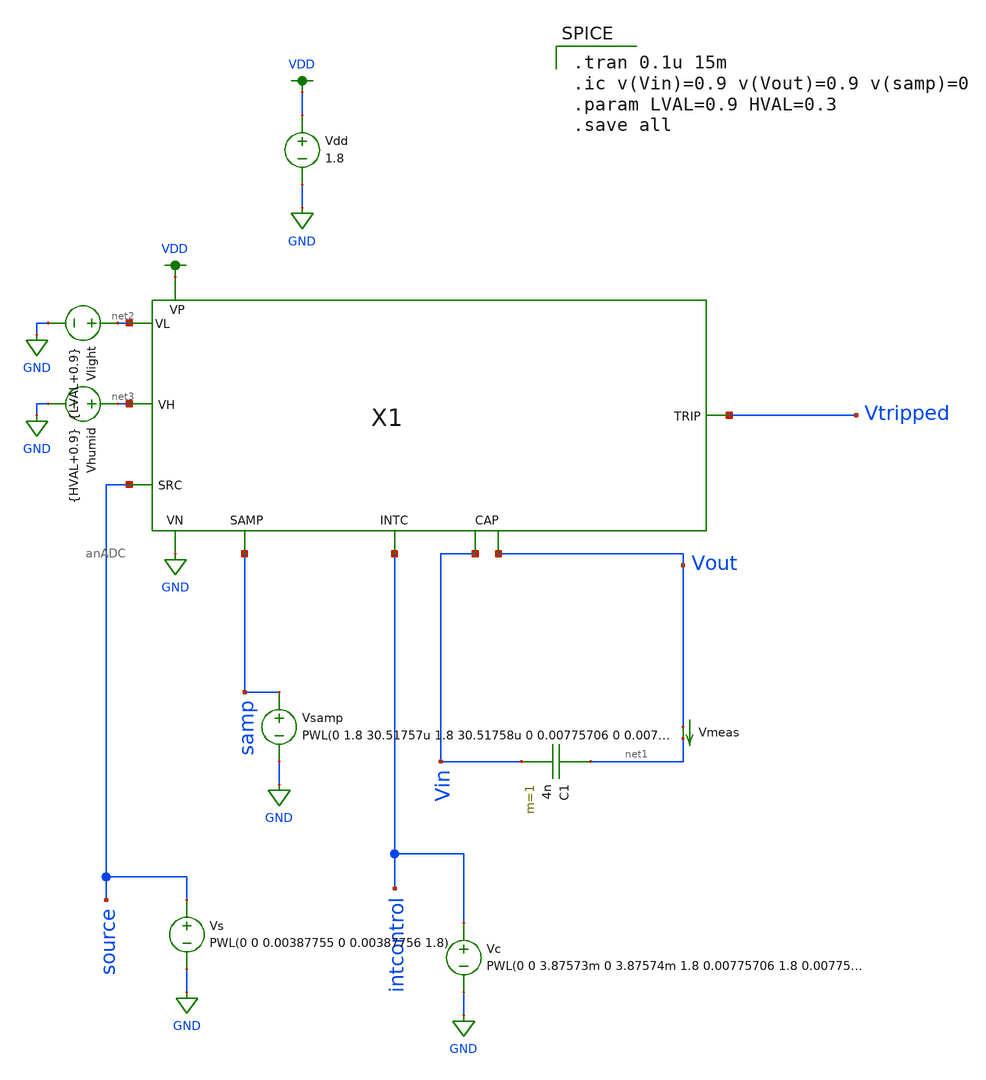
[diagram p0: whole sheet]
** sch_path: analog/anADC_test.sch
**.subckt anADC_test
Vdd VDD GND 1.8
C1 net1 Vin 4n m=1
Vlight net2 GND {LVAL+0.9}
Vmeas Vout net1 0
.save i(vmeas)
Vhumid net3 GND {HVAL+0.9}
Vs source GND PWL(0 0 0.00387755 0 0.00387756 1.8)
Vc intcontrol GND PWL(0 0 3.87573m 0 3.87574m 1.8 0.00775706 1.8 0.007757061 0 0.01163461 0
+ 0.01163462 1.8)
Vsamp samp GND PWL(0 1.8 30.51757u 1.8 30.51758u 0 0.00775706 0 0.007757061 1.8 0.00778757 1.8
+ 0.00778758 0)
X1 Vtripped Vout Vin intcontrol samp source net3 net2 anADC
**** begin user architecture code

.option wnflag=1
.param MC_SWITCH=0.0
.lib ~/skywater/skywater-pdk/libraries/sky130_fd_pr_ngspice/latest/models/sky130.lib.spice tt


.tran 0.1u 15m
.ic v(Vin)=0.9 v(Vout)=0.9 v(samp)=0
.param LVAL=0.9 HVAL=0.3
.save all

**** end user architecture code
**.ends

* expanding   symbol:  /home/jonah/VLSI/final/anADC.sym # of pins=8
** sym_path: analog/anADC.sym
** sch_path: analog/anADC.sch
.subckt anADC Vtrip OCC2 OCC1 intc Samp Source VH VL
*.iopin OCC1
*.iopin OCC2
*.iopin VL
*.iopin VH
*.ipin Samp
*.ipin Source
*.ipin intc
*.opin Vtrip
X4 net1 OCC2 net10 net3 GND VDD sbc2
X7 net1 OCC1 net2 OCC2 GND VDD sbc2
XM5 VDD net3 Vtrip VDD sky130_fd_pr__pfet_01v8 L=0.15 W=3 nf=1 ad='int((nf+1)/2) * W/nf * 0.29' as='int((nf+2)/2) * W/nf * 0.29'
+ pd='2*int((nf+1)/2) * (W/nf + 0.29)' ps='2*int((nf+2)/2) * (W/nf + 0.29)' nrd='0.29 / W' nrs='0.29 / W'
+ sa=0 sb=0 sd=0 mult=1 m=1
XM6 Vtrip net3 GND GND sky130_fd_pr__nfet_01v8 L=0.15 W=3 nf=1 ad='int((nf+1)/2) * W/nf * 0.29' as='int((nf+2)/2) * W/nf * 0.29'
+ pd='2*int((nf+1)/2) * (W/nf + 0.29)' ps='2*int((nf+2)/2) * (W/nf + 0.29)' nrd='0.29 / W' nrs='0.29 / W'
+ sa=0 sb=0 sd=0 mult=1 m=1
X8 net5 GND net4 VDD GND intc amux
X9 net8 net5 net6 net5 GND VDD sbc2
XR1 OCC1 net4 GND sky130_fd_pr__res_xhigh_po W=0.35 L=175.2 mult=1 m=1
XR2 net1 VDD GND sky130_fd_pr__res_xhigh_po W=0.35 L=194 mult=1 m=1
XR3 GND net1 GND sky130_fd_pr__res_xhigh_po W=0.35 L=194 mult=1 m=1
XM3 net7 Samp net8 GND sky130_fd_pr__nfet_01v8 L=0.15 W=5 nf=1 ad='int((nf+1)/2) * W/nf * 0.29' as='int((nf+2)/2) * W/nf * 0.29'
+ pd='2*int((nf+1)/2) * (W/nf + 0.29)' ps='2*int((nf+2)/2) * (W/nf + 0.29)' nrd='0.29 / W' nrs='0.29 / W'
+ sa=0 sb=0 sd=0 mult=1 m=1
X6 VL VH net7 VDD GND Source amux
XM4 net7 net9 net8 VDD sky130_fd_pr__pfet_01v8 L=0.15 W=5 nf=1 ad='int((nf+1)/2) * W/nf * 0.29' as='int((nf+2)/2) * W/nf * 0.29'
+ pd='2*int((nf+1)/2) * (W/nf + 0.29)' ps='2*int((nf+2)/2) * (W/nf + 0.29)' nrd='0.29 / W' nrs='0.29 / W'
+ sa=0 sb=0 sd=0 mult=1 m=1
XM1 GND Samp net9 GND sky130_fd_pr__nfet_01v8 L=0.15 W=1 nf=1 ad='int((nf+1)/2) * W/nf * 0.29' as='int((nf+2)/2) * W/nf * 0.29'
+ pd='2*int((nf+1)/2) * (W/nf + 0.29)' ps='2*int((nf+2)/2) * (W/nf + 0.29)' nrd='0.29 / W' nrs='0.29 / W'
+ sa=0 sb=0 sd=0 mult=1 m=1
XM2 VDD Samp net9 VDD sky130_fd_pr__pfet_01v8 L=0.15 W=1 nf=1 ad='int((nf+1)/2) * W/nf * 0.29' as='int((nf+2)/2) * W/nf * 0.29'
+ pd='2*int((nf+1)/2) * (W/nf + 0.29)' ps='2*int((nf+2)/2) * (W/nf + 0.29)' nrd='0.29 / W' nrs='0.29 / W'
+ sa=0 sb=0 sd=0 mult=1 m=1
XC2 net2 OCC2 sky130_fd_pr__cap_mim_m3_1 W=25 L=10 MF=1 m=1
XC1 net5 net6 sky130_fd_pr__cap_mim_m3_1 W=25 L=10 MF=1 m=1
XC3 net8 GND sky130_fd_pr__cap_mim_m3_1 W=25 L=20 MF=1 m=1
.ends


* expanding   symbol:  /home/jonah/VLSI/final/sbc2.sym # of pins=6
** sym_path: analog/sbc2.sym
** sch_path: analog/sbc2.sch
.subckt sbc2 V1 V2 nVout Vout VN VP
*.ipin V1
*.ipin V2
*.iopin Vout
*.iopin nVout
*.iopin VP
*.iopin VN
XM7a net2 V1 net1 GND sky130_fd_pr__nfet_01v8 L=0.6 W=1.5 nf=1 ad='int((nf+1)/2) * W/nf * 0.29' as='int((nf+2)/2) * W/nf * 0.29'
+ pd='2*int((nf+1)/2) * (W/nf + 0.29)' ps='2*int((nf+2)/2) * (W/nf + 0.29)' nrd='0.29 / W' nrs='0.29 / W'
+ sa=0 sb=0 sd=0 mult=1 m=1
XM8a net3 V2 net2 GND sky130_fd_pr__nfet_01v8 L=0.6 W=1.5 nf=1 ad='int((nf+1)/2) * W/nf * 0.29' as='int((nf+2)/2) * W/nf * 0.29'
+ pd='2*int((nf+1)/2) * (W/nf + 0.29)' ps='2*int((nf+2)/2) * (W/nf + 0.29)' nrd='0.29 / W' nrs='0.29 / W'
+ sa=0 sb=0 sd=0 mult=1 m=1
XM8b net2 V2 net3 GND sky130_fd_pr__nfet_01v8 L=0.6 W=1.5 nf=1 ad='int((nf+1)/2) * W/nf * 0.29' as='int((nf+2)/2) * W/nf * 0.29'
+ pd='2*int((nf+1)/2) * (W/nf + 0.29)' ps='2*int((nf+2)/2) * (W/nf + 0.29)' nrd='0.29 / W' nrs='0.29 / W'
+ sa=0 sb=0 sd=0 mult=1 m=1
XM7b net1 V1 net2 GND sky130_fd_pr__nfet_01v8 L=0.6 W=1.5 nf=1 ad='int((nf+1)/2) * W/nf * 0.29' as='int((nf+2)/2) * W/nf * 0.29'
+ pd='2*int((nf+1)/2) * (W/nf + 0.29)' ps='2*int((nf+2)/2) * (W/nf + 0.29)' nrd='0.29 / W' nrs='0.29 / W'
+ sa=0 sb=0 sd=0 mult=1 m=1
XMd1 net1 VN VN GND sky130_fd_pr__nfet_01v8 L=0.6 W=1.5 nf=1 ad='int((nf+1)/2) * W/nf * 0.29' as='int((nf+2)/2) * W/nf * 0.29'
+ pd='2*int((nf+1)/2) * (W/nf + 0.29)' ps='2*int((nf+2)/2) * (W/nf + 0.29)' nrd='0.29 / W' nrs='0.29 / W'
+ sa=0 sb=0 sd=0 mult=1 m=1
XMd2 VN VN net1 GND sky130_fd_pr__nfet_01v8 L=0.6 W=1.5 nf=1 ad='int((nf+1)/2) * W/nf * 0.29' as='int((nf+2)/2) * W/nf * 0.29'
+ pd='2*int((nf+1)/2) * (W/nf + 0.29)' ps='2*int((nf+2)/2) * (W/nf + 0.29)' nrd='0.29 / W' nrs='0.29 / W'
+ sa=0 sb=0 sd=0 mult=1 m=1
XMd3 VP VP net4 VDD sky130_fd_pr__pfet_01v8 L=0.6 W=1.5 nf=1 ad='int((nf+1)/2) * W/nf * 0.29' as='int((nf+2)/2) * W/nf * 0.29'
+ pd='2*int((nf+1)/2) * (W/nf + 0.29)' ps='2*int((nf+2)/2) * (W/nf + 0.29)' nrd='0.29 / W' nrs='0.29 / W'
+ sa=0 sb=0 sd=0 mult=1 m=1
XM15a net4 V2 net5 VDD sky130_fd_pr__pfet_01v8 L=0.6 W=1.5 nf=1 ad='int((nf+1)/2) * W/nf * 0.29' as='int((nf+2)/2) * W/nf * 0.29'
+ pd='2*int((nf+1)/2) * (W/nf + 0.29)' ps='2*int((nf+2)/2) * (W/nf + 0.29)' nrd='0.29 / W' nrs='0.29 / W'
+ sa=0 sb=0 sd=0 mult=1 m=1
XM16a net5 V1 net6 VDD sky130_fd_pr__pfet_01v8 L=0.6 W=1.5 nf=1 ad='int((nf+1)/2) * W/nf * 0.29' as='int((nf+2)/2) * W/nf * 0.29'
+ pd='2*int((nf+1)/2) * (W/nf + 0.29)' ps='2*int((nf+2)/2) * (W/nf + 0.29)' nrd='0.29 / W' nrs='0.29 / W'
+ sa=0 sb=0 sd=0 mult=1 m=1
XM16b net6 V1 net5 VDD sky130_fd_pr__pfet_01v8 L=0.6 W=1.5 nf=1 ad='int((nf+1)/2) * W/nf * 0.29' as='int((nf+2)/2) * W/nf * 0.29'
+ pd='2*int((nf+1)/2) * (W/nf + 0.29)' ps='2*int((nf+2)/2) * (W/nf + 0.29)' nrd='0.29 / W' nrs='0.29 / W'
+ sa=0 sb=0 sd=0 mult=1 m=1
XM15b net5 V2 net4 VDD sky130_fd_pr__pfet_01v8 L=0.6 W=1.5 nf=1 ad='int((nf+1)/2) * W/nf * 0.29' as='int((nf+2)/2) * W/nf * 0.29'
+ pd='2*int((nf+1)/2) * (W/nf + 0.29)' ps='2*int((nf+2)/2) * (W/nf + 0.29)' nrd='0.29 / W' nrs='0.29 / W'
+ sa=0 sb=0 sd=0 mult=1 m=1
XMd4 net4 VP VP VDD sky130_fd_pr__pfet_01v8 L=0.6 W=1.5 nf=1 ad='int((nf+1)/2) * W/nf * 0.29' as='int((nf+2)/2) * W/nf * 0.29'
+ pd='2*int((nf+1)/2) * (W/nf + 0.29)' ps='2*int((nf+2)/2) * (W/nf + 0.29)' nrd='0.29 / W' nrs='0.29 / W'
+ sa=0 sb=0 sd=0 mult=1 m=1
XM20a net8 net9 net7 VDD sky130_fd_pr__pfet_01v8 L=0.6 W=1.5 nf=1 ad='int((nf+1)/2) * W/nf * 0.29' as='int((nf+2)/2) * W/nf * 0.29'
+ pd='2*int((nf+1)/2) * (W/nf + 0.29)' ps='2*int((nf+2)/2) * (W/nf + 0.29)' nrd='0.29 / W' nrs='0.29 / W'
+ sa=0 sb=0 sd=0 mult=1 m=1
XM21a net7 net9 VP VDD sky130_fd_pr__pfet_01v8 L=0.6 W=1.5 nf=1 ad='int((nf+1)/2) * W/nf * 0.29' as='int((nf+2)/2) * W/nf * 0.29'
+ pd='2*int((nf+1)/2) * (W/nf + 0.29)' ps='2*int((nf+2)/2) * (W/nf + 0.29)' nrd='0.29 / W' nrs='0.29 / W'
+ sa=0 sb=0 sd=0 mult=1 m=1
XM14a VP net9 net6 VDD sky130_fd_pr__pfet_01v8 L=0.6 W=1.5 nf=1 ad='int((nf+1)/2) * W/nf * 0.29' as='int((nf+2)/2) * W/nf * 0.29'
+ pd='2*int((nf+1)/2) * (W/nf + 0.29)' ps='2*int((nf+2)/2) * (W/nf + 0.29)' nrd='0.29 / W' nrs='0.29 / W'
+ sa=0 sb=0 sd=0 mult=1 m=1
XM14b net6 net9 VP VDD sky130_fd_pr__pfet_01v8 L=0.6 W=1.5 nf=1 ad='int((nf+1)/2) * W/nf * 0.29' as='int((nf+2)/2) * W/nf * 0.29'
+ pd='2*int((nf+1)/2) * (W/nf + 0.29)' ps='2*int((nf+2)/2) * (W/nf + 0.29)' nrd='0.29 / W' nrs='0.29 / W'
+ sa=0 sb=0 sd=0 mult=1 m=1
XM21b VP net9 net7 VDD sky130_fd_pr__pfet_01v8 L=0.6 W=1.5 nf=1 ad='int((nf+1)/2) * W/nf * 0.29' as='int((nf+2)/2) * W/nf * 0.29'
+ pd='2*int((nf+1)/2) * (W/nf + 0.29)' ps='2*int((nf+2)/2) * (W/nf + 0.29)' nrd='0.29 / W' nrs='0.29 / W'
+ sa=0 sb=0 sd=0 mult=1 m=1
XM20b net7 net9 net8 VDD sky130_fd_pr__pfet_01v8 L=0.6 W=1.5 nf=1 ad='int((nf+1)/2) * W/nf * 0.29' as='int((nf+2)/2) * W/nf * 0.29'
+ pd='2*int((nf+1)/2) * (W/nf + 0.29)' ps='2*int((nf+2)/2) * (W/nf + 0.29)' nrd='0.29 / W' nrs='0.29 / W'
+ sa=0 sb=0 sd=0 mult=1 m=1
XMd5 net8 VP VP VDD sky130_fd_pr__pfet_01v8 L=0.6 W=1.5 nf=1 ad='int((nf+1)/2) * W/nf * 0.29' as='int((nf+2)/2) * W/nf * 0.29'
+ pd='2*int((nf+1)/2) * (W/nf + 0.29)' ps='2*int((nf+2)/2) * (W/nf + 0.29)' nrd='0.29 / W' nrs='0.29 / W'
+ sa=0 sb=0 sd=0 mult=1 m=1
XMd6 VP VP net8 VDD sky130_fd_pr__pfet_01v8 L=0.6 W=1.5 nf=1 ad='int((nf+1)/2) * W/nf * 0.29' as='int((nf+2)/2) * W/nf * 0.29'
+ pd='2*int((nf+1)/2) * (W/nf + 0.29)' ps='2*int((nf+2)/2) * (W/nf + 0.29)' nrd='0.29 / W' nrs='0.29 / W'
+ sa=0 sb=0 sd=0 mult=1 m=1
XM22a VN net9 net7 VDD sky130_fd_pr__pfet_01v8 L=0.6 W=1.5 nf=1 ad='int((nf+1)/2) * W/nf * 0.29' as='int((nf+2)/2) * W/nf * 0.29'
+ pd='2*int((nf+1)/2) * (W/nf + 0.29)' ps='2*int((nf+2)/2) * (W/nf + 0.29)' nrd='0.29 / W' nrs='0.29 / W'
+ sa=0 sb=0 sd=0 mult=1 m=1
XM22b net7 net9 VN VDD sky130_fd_pr__pfet_01v8 L=0.6 W=1.5 nf=1 ad='int((nf+1)/2) * W/nf * 0.29' as='int((nf+2)/2) * W/nf * 0.29'
+ pd='2*int((nf+1)/2) * (W/nf + 0.29)' ps='2*int((nf+2)/2) * (W/nf + 0.29)' nrd='0.29 / W' nrs='0.29 / W'
+ sa=0 sb=0 sd=0 mult=1 m=1
XM22c VN net9 net7 VDD sky130_fd_pr__pfet_01v8 L=0.6 W=1.5 nf=1 ad='int((nf+1)/2) * W/nf * 0.29' as='int((nf+2)/2) * W/nf * 0.29'
+ pd='2*int((nf+1)/2) * (W/nf + 0.29)' ps='2*int((nf+2)/2) * (W/nf + 0.29)' nrd='0.29 / W' nrs='0.29 / W'
+ sa=0 sb=0 sd=0 mult=1 m=1
XM22d net7 net9 VN VDD sky130_fd_pr__pfet_01v8 L=0.6 W=1.5 nf=1 ad='int((nf+1)/2) * W/nf * 0.29' as='int((nf+2)/2) * W/nf * 0.29'
+ pd='2*int((nf+1)/2) * (W/nf + 0.29)' ps='2*int((nf+2)/2) * (W/nf + 0.29)' nrd='0.29 / W' nrs='0.29 / W'
+ sa=0 sb=0 sd=0 mult=1 m=1
XM22e VN net9 net7 VDD sky130_fd_pr__pfet_01v8 L=0.6 W=1.5 nf=1 ad='int((nf+1)/2) * W/nf * 0.29' as='int((nf+2)/2) * W/nf * 0.29'
+ pd='2*int((nf+1)/2) * (W/nf + 0.29)' ps='2*int((nf+2)/2) * (W/nf + 0.29)' nrd='0.29 / W' nrs='0.29 / W'
+ sa=0 sb=0 sd=0 mult=1 m=1
XM22f net7 net9 VN VDD sky130_fd_pr__pfet_01v8 L=0.6 W=1.5 nf=1 ad='int((nf+1)/2) * W/nf * 0.29' as='int((nf+2)/2) * W/nf * 0.29'
+ pd='2*int((nf+1)/2) * (W/nf + 0.29)' ps='2*int((nf+2)/2) * (W/nf + 0.29)' nrd='0.29 / W' nrs='0.29 / W'
+ sa=0 sb=0 sd=0 mult=1 m=1
XMd7 VN VP VP VDD sky130_fd_pr__pfet_01v8 L=0.6 W=1.5 nf=1 ad='int((nf+1)/2) * W/nf * 0.29' as='int((nf+2)/2) * W/nf * 0.29'
+ pd='2*int((nf+1)/2) * (W/nf + 0.29)' ps='2*int((nf+2)/2) * (W/nf + 0.29)' nrd='0.29 / W' nrs='0.29 / W'
+ sa=0 sb=0 sd=0 mult=1 m=1
XMd8 VP VP VN VDD sky130_fd_pr__pfet_01v8 L=0.6 W=1.5 nf=1 ad='int((nf+1)/2) * W/nf * 0.29' as='int((nf+2)/2) * W/nf * 0.29'
+ pd='2*int((nf+1)/2) * (W/nf + 0.29)' ps='2*int((nf+2)/2) * (W/nf + 0.29)' nrd='0.29 / W' nrs='0.29 / W'
+ sa=0 sb=0 sd=0 mult=1 m=1
XM18a net10 net8 net9 GND sky130_fd_pr__nfet_01v8 L=0.6 W=1.5 nf=1 ad='int((nf+1)/2) * W/nf * 0.29' as='int((nf+2)/2) * W/nf * 0.29'
+ pd='2*int((nf+1)/2) * (W/nf + 0.29)' ps='2*int((nf+2)/2) * (W/nf + 0.29)' nrd='0.29 / W' nrs='0.29 / W'
+ sa=0 sb=0 sd=0 mult=1 m=1
XM17a VN net8 net10 GND sky130_fd_pr__nfet_01v8 L=0.6 W=1.5 nf=1 ad='int((nf+1)/2) * W/nf * 0.29' as='int((nf+2)/2) * W/nf * 0.29'
+ pd='2*int((nf+1)/2) * (W/nf + 0.29)' ps='2*int((nf+2)/2) * (W/nf + 0.29)' nrd='0.29 / W' nrs='0.29 / W'
+ sa=0 sb=0 sd=0 mult=1 m=1
XM6a net2 net8 VN GND sky130_fd_pr__nfet_01v8 L=0.6 W=1.5 nf=1 ad='int((nf+1)/2) * W/nf * 0.29' as='int((nf+2)/2) * W/nf * 0.29'
+ pd='2*int((nf+1)/2) * (W/nf + 0.29)' ps='2*int((nf+2)/2) * (W/nf + 0.29)' nrd='0.29 / W' nrs='0.29 / W'
+ sa=0 sb=0 sd=0 mult=1 m=1
XM6b VN net8 net2 GND sky130_fd_pr__nfet_01v8 L=0.6 W=1.5 nf=1 ad='int((nf+1)/2) * W/nf * 0.29' as='int((nf+2)/2) * W/nf * 0.29'
+ pd='2*int((nf+1)/2) * (W/nf + 0.29)' ps='2*int((nf+2)/2) * (W/nf + 0.29)' nrd='0.29 / W' nrs='0.29 / W'
+ sa=0 sb=0 sd=0 mult=1 m=1
XMd9 net9 VN VN GND sky130_fd_pr__nfet_01v8 L=0.6 W=1.5 nf=1 ad='int((nf+1)/2) * W/nf * 0.29' as='int((nf+2)/2) * W/nf * 0.29'
+ pd='2*int((nf+1)/2) * (W/nf + 0.29)' ps='2*int((nf+2)/2) * (W/nf + 0.29)' nrd='0.29 / W' nrs='0.29 / W'
+ sa=0 sb=0 sd=0 mult=1 m=1
XM17b net10 net8 VN GND sky130_fd_pr__nfet_01v8 L=0.6 W=1.5 nf=1 ad='int((nf+1)/2) * W/nf * 0.29' as='int((nf+2)/2) * W/nf * 0.29'
+ pd='2*int((nf+1)/2) * (W/nf + 0.29)' ps='2*int((nf+2)/2) * (W/nf + 0.29)' nrd='0.29 / W' nrs='0.29 / W'
+ sa=0 sb=0 sd=0 mult=1 m=1
XM18b net9 net8 net10 GND sky130_fd_pr__nfet_01v8 L=0.6 W=1.5 nf=1 ad='int((nf+1)/2) * W/nf * 0.29' as='int((nf+2)/2) * W/nf * 0.29'
+ pd='2*int((nf+1)/2) * (W/nf + 0.29)' ps='2*int((nf+2)/2) * (W/nf + 0.29)' nrd='0.29 / W' nrs='0.29 / W'
+ sa=0 sb=0 sd=0 mult=1 m=1
XMd10 VN VN net9 GND sky130_fd_pr__nfet_01v8 L=0.6 W=1.5 nf=1 ad='int((nf+1)/2) * W/nf * 0.29' as='int((nf+2)/2) * W/nf * 0.29'
+ pd='2*int((nf+1)/2) * (W/nf + 0.29)' ps='2*int((nf+2)/2) * (W/nf + 0.29)' nrd='0.29 / W' nrs='0.29 / W'
+ sa=0 sb=0 sd=0 mult=1 m=1
XM19a net10 net8 VP GND sky130_fd_pr__nfet_01v8 L=0.6 W=1.5 nf=1 ad='int((nf+1)/2) * W/nf * 0.29' as='int((nf+2)/2) * W/nf * 0.29'
+ pd='2*int((nf+1)/2) * (W/nf + 0.29)' ps='2*int((nf+2)/2) * (W/nf + 0.29)' nrd='0.29 / W' nrs='0.29 / W'
+ sa=0 sb=0 sd=0 mult=1 m=1
XM19b VP net8 net10 GND sky130_fd_pr__nfet_01v8 L=0.6 W=1.5 nf=1 ad='int((nf+1)/2) * W/nf * 0.29' as='int((nf+2)/2) * W/nf * 0.29'
+ pd='2*int((nf+1)/2) * (W/nf + 0.29)' ps='2*int((nf+2)/2) * (W/nf + 0.29)' nrd='0.29 / W' nrs='0.29 / W'
+ sa=0 sb=0 sd=0 mult=1 m=1
XM19c net10 net8 VP GND sky130_fd_pr__nfet_01v8 L=0.6 W=1.5 nf=1 ad='int((nf+1)/2) * W/nf * 0.29' as='int((nf+2)/2) * W/nf * 0.29'
+ pd='2*int((nf+1)/2) * (W/nf + 0.29)' ps='2*int((nf+2)/2) * (W/nf + 0.29)' nrd='0.29 / W' nrs='0.29 / W'
+ sa=0 sb=0 sd=0 mult=1 m=1
XM19d VP net8 net10 GND sky130_fd_pr__nfet_01v8 L=0.6 W=1.5 nf=1 ad='int((nf+1)/2) * W/nf * 0.29' as='int((nf+2)/2) * W/nf * 0.29'
+ pd='2*int((nf+1)/2) * (W/nf + 0.29)' ps='2*int((nf+2)/2) * (W/nf + 0.29)' nrd='0.29 / W' nrs='0.29 / W'
+ sa=0 sb=0 sd=0 mult=1 m=1
XMd11 VP VN VN GND sky130_fd_pr__nfet_01v8 L=0.6 W=1.5 nf=1 ad='int((nf+1)/2) * W/nf * 0.29' as='int((nf+2)/2) * W/nf * 0.29'
+ pd='2*int((nf+1)/2) * (W/nf + 0.29)' ps='2*int((nf+2)/2) * (W/nf + 0.29)' nrd='0.29 / W' nrs='0.29 / W'
+ sa=0 sb=0 sd=0 mult=1 m=1
XM19e net10 net8 VP GND sky130_fd_pr__nfet_01v8 L=0.6 W=1.5 nf=1 ad='int((nf+1)/2) * W/nf * 0.29' as='int((nf+2)/2) * W/nf * 0.29'
+ pd='2*int((nf+1)/2) * (W/nf + 0.29)' ps='2*int((nf+2)/2) * (W/nf + 0.29)' nrd='0.29 / W' nrs='0.29 / W'
+ sa=0 sb=0 sd=0 mult=1 m=1
XM19f VP net8 net10 GND sky130_fd_pr__nfet_01v8 L=0.6 W=1.5 nf=1 ad='int((nf+1)/2) * W/nf * 0.29' as='int((nf+2)/2) * W/nf * 0.29'
+ pd='2*int((nf+1)/2) * (W/nf + 0.29)' ps='2*int((nf+2)/2) * (W/nf + 0.29)' nrd='0.29 / W' nrs='0.29 / W'
+ sa=0 sb=0 sd=0 mult=1 m=1
XMd14 VN VN VP GND sky130_fd_pr__nfet_01v8 L=0.6 W=1.5 nf=1 ad='int((nf+1)/2) * W/nf * 0.29' as='int((nf+2)/2) * W/nf * 0.29'
+ pd='2*int((nf+1)/2) * (W/nf + 0.29)' ps='2*int((nf+2)/2) * (W/nf + 0.29)' nrd='0.29 / W' nrs='0.29 / W'
+ sa=0 sb=0 sd=0 mult=1 m=1
XM13a net3 net9 net9 VDD sky130_fd_pr__pfet_01v8 L=0.6 W=1.5 nf=1 ad='int((nf+1)/2) * W/nf * 0.29' as='int((nf+2)/2) * W/nf * 0.29'
+ pd='2*int((nf+1)/2) * (W/nf + 0.29)' ps='2*int((nf+2)/2) * (W/nf + 0.29)' nrd='0.29 / W' nrs='0.29 / W'
+ sa=0 sb=0 sd=0 mult=1 m=1
XM13b net9 net9 net3 VDD sky130_fd_pr__pfet_01v8 L=0.6 W=1.5 nf=1 ad='int((nf+1)/2) * W/nf * 0.29' as='int((nf+2)/2) * W/nf * 0.29'
+ pd='2*int((nf+1)/2) * (W/nf + 0.29)' ps='2*int((nf+2)/2) * (W/nf + 0.29)' nrd='0.29 / W' nrs='0.29 / W'
+ sa=0 sb=0 sd=0 mult=1 m=1
XM10a net3 net9 VP VDD sky130_fd_pr__pfet_01v8 L=0.6 W=1.5 nf=1 ad='int((nf+1)/2) * W/nf * 0.29' as='int((nf+2)/2) * W/nf * 0.29'
+ pd='2*int((nf+1)/2) * (W/nf + 0.29)' ps='2*int((nf+2)/2) * (W/nf + 0.29)' nrd='0.29 / W' nrs='0.29 / W'
+ sa=0 sb=0 sd=0 mult=1 m=1
XM9a VP net9 net1 VDD sky130_fd_pr__pfet_01v8 L=0.6 W=1.5 nf=1 ad='int((nf+1)/2) * W/nf * 0.29' as='int((nf+2)/2) * W/nf * 0.29'
+ pd='2*int((nf+1)/2) * (W/nf + 0.29)' ps='2*int((nf+2)/2) * (W/nf + 0.29)' nrd='0.29 / W' nrs='0.29 / W'
+ sa=0 sb=0 sd=0 mult=1 m=1
XM9b net1 net9 VP VDD sky130_fd_pr__pfet_01v8 L=0.6 W=1.5 nf=1 ad='int((nf+1)/2) * W/nf * 0.29' as='int((nf+2)/2) * W/nf * 0.29'
+ pd='2*int((nf+1)/2) * (W/nf + 0.29)' ps='2*int((nf+2)/2) * (W/nf + 0.29)' nrd='0.29 / W' nrs='0.29 / W'
+ sa=0 sb=0 sd=0 mult=1 m=1
XM10b VP net9 net3 VDD sky130_fd_pr__pfet_01v8 L=0.6 W=1.5 nf=1 ad='int((nf+1)/2) * W/nf * 0.29' as='int((nf+2)/2) * W/nf * 0.29'
+ pd='2*int((nf+1)/2) * (W/nf + 0.29)' ps='2*int((nf+2)/2) * (W/nf + 0.29)' nrd='0.29 / W' nrs='0.29 / W'
+ sa=0 sb=0 sd=0 mult=1 m=1
XMd12 VP VP net3 VDD sky130_fd_pr__pfet_01v8 L=0.6 W=1.5 nf=1 ad='int((nf+1)/2) * W/nf * 0.29' as='int((nf+2)/2) * W/nf * 0.29'
+ pd='2*int((nf+1)/2) * (W/nf + 0.29)' ps='2*int((nf+2)/2) * (W/nf + 0.29)' nrd='0.29 / W' nrs='0.29 / W'
+ sa=0 sb=0 sd=0 mult=1 m=1
XMd13 net3 VP VP VDD sky130_fd_pr__pfet_01v8 L=0.6 W=1.5 nf=1 ad='int((nf+1)/2) * W/nf * 0.29' as='int((nf+2)/2) * W/nf * 0.29'
+ pd='2*int((nf+1)/2) * (W/nf + 0.29)' ps='2*int((nf+2)/2) * (W/nf + 0.29)' nrd='0.29 / W' nrs='0.29 / W'
+ sa=0 sb=0 sd=0 mult=1 m=1
XM5a net8 net8 net4 GND sky130_fd_pr__nfet_01v8 L=0.6 W=1.5 nf=1 ad='int((nf+1)/2) * W/nf * 0.29' as='int((nf+2)/2) * W/nf * 0.29'
+ pd='2*int((nf+1)/2) * (W/nf + 0.29)' ps='2*int((nf+2)/2) * (W/nf + 0.29)' nrd='0.29 / W' nrs='0.29 / W'
+ sa=0 sb=0 sd=0 mult=1 m=1
XM5b net4 net8 net8 GND sky130_fd_pr__nfet_01v8 L=0.6 W=1.5 nf=1 ad='int((nf+1)/2) * W/nf * 0.29' as='int((nf+2)/2) * W/nf * 0.29'
+ pd='2*int((nf+1)/2) * (W/nf + 0.29)' ps='2*int((nf+2)/2) * (W/nf + 0.29)' nrd='0.29 / W' nrs='0.29 / W'
+ sa=0 sb=0 sd=0 mult=1 m=1
XM2a VN net8 net4 GND sky130_fd_pr__nfet_01v8 L=0.6 W=1.5 nf=1 ad='int((nf+1)/2) * W/nf * 0.29' as='int((nf+2)/2) * W/nf * 0.29'
+ pd='2*int((nf+1)/2) * (W/nf + 0.29)' ps='2*int((nf+2)/2) * (W/nf + 0.29)' nrd='0.29 / W' nrs='0.29 / W'
+ sa=0 sb=0 sd=0 mult=1 m=1
XM1a net5 net8 VN GND sky130_fd_pr__nfet_01v8 L=0.6 W=1.5 nf=1 ad='int((nf+1)/2) * W/nf * 0.29' as='int((nf+2)/2) * W/nf * 0.29'
+ pd='2*int((nf+1)/2) * (W/nf + 0.29)' ps='2*int((nf+2)/2) * (W/nf + 0.29)' nrd='0.29 / W' nrs='0.29 / W'
+ sa=0 sb=0 sd=0 mult=1 m=1
XMd15 net4 VN VN GND sky130_fd_pr__nfet_01v8 L=0.6 W=1.5 nf=1 ad='int((nf+1)/2) * W/nf * 0.29' as='int((nf+2)/2) * W/nf * 0.29'
+ pd='2*int((nf+1)/2) * (W/nf + 0.29)' ps='2*int((nf+2)/2) * (W/nf + 0.29)' nrd='0.29 / W' nrs='0.29 / W'
+ sa=0 sb=0 sd=0 mult=1 m=1
XM1b VN net8 net5 GND sky130_fd_pr__nfet_01v8 L=0.6 W=1.5 nf=1 ad='int((nf+1)/2) * W/nf * 0.29' as='int((nf+2)/2) * W/nf * 0.29'
+ pd='2*int((nf+1)/2) * (W/nf + 0.29)' ps='2*int((nf+2)/2) * (W/nf + 0.29)' nrd='0.29 / W' nrs='0.29 / W'
+ sa=0 sb=0 sd=0 mult=1 m=1
XM2b net4 net8 VN GND sky130_fd_pr__nfet_01v8 L=0.6 W=1.5 nf=1 ad='int((nf+1)/2) * W/nf * 0.29' as='int((nf+2)/2) * W/nf * 0.29'
+ pd='2*int((nf+1)/2) * (W/nf + 0.29)' ps='2*int((nf+2)/2) * (W/nf + 0.29)' nrd='0.29 / W' nrs='0.29 / W'
+ sa=0 sb=0 sd=0 mult=1 m=1
XMd18 VN VN net4 GND sky130_fd_pr__nfet_01v8 L=0.6 W=1.5 nf=1 ad='int((nf+1)/2) * W/nf * 0.29' as='int((nf+2)/2) * W/nf * 0.29'
+ pd='2*int((nf+1)/2) * (W/nf + 0.29)' ps='2*int((nf+2)/2) * (W/nf + 0.29)' nrd='0.29 / W' nrs='0.29 / W'
+ sa=0 sb=0 sd=0 mult=1 m=1
XM12a net3 net11 net11 VDD sky130_fd_pr__pfet_01v8 L=0.6 W=1.5 nf=1 ad='int((nf+1)/2) * W/nf * 0.29'
+ as='int((nf+2)/2) * W/nf * 0.29' pd='2*int((nf+1)/2) * (W/nf + 0.29)' ps='2*int((nf+2)/2) * (W/nf + 0.29)'
+ nrd='0.29 / W' nrs='0.29 / W' sa=0 sb=0 sd=0 mult=1 m=1
XM11a nVout net11 net1 VDD sky130_fd_pr__pfet_01v8 L=0.6 W=1.5 nf=1 ad='int((nf+1)/2) * W/nf * 0.29'
+ as='int((nf+2)/2) * W/nf * 0.29' pd='2*int((nf+1)/2) * (W/nf + 0.29)' ps='2*int((nf+2)/2) * (W/nf + 0.29)'
+ nrd='0.29 / W' nrs='0.29 / W' sa=0 sb=0 sd=0 mult=1 m=1
XM11b net1 net11 nVout VDD sky130_fd_pr__pfet_01v8 L=0.6 W=1.5 nf=1 ad='int((nf+1)/2) * W/nf * 0.29'
+ as='int((nf+2)/2) * W/nf * 0.29' pd='2*int((nf+1)/2) * (W/nf + 0.29)' ps='2*int((nf+2)/2) * (W/nf + 0.29)'
+ nrd='0.29 / W' nrs='0.29 / W' sa=0 sb=0 sd=0 mult=1 m=1
XM12b net11 net11 net3 VDD sky130_fd_pr__pfet_01v8 L=0.6 W=1.5 nf=1 ad='int((nf+1)/2) * W/nf * 0.29'
+ as='int((nf+2)/2) * W/nf * 0.29' pd='2*int((nf+1)/2) * (W/nf + 0.29)' ps='2*int((nf+2)/2) * (W/nf + 0.29)'
+ nrd='0.29 / W' nrs='0.29 / W' sa=0 sb=0 sd=0 mult=1 m=1
XMd16 net3 VP VP VDD sky130_fd_pr__pfet_01v8 L=0.6 W=1.5 nf=1 ad='int((nf+1)/2) * W/nf * 0.29' as='int((nf+2)/2) * W/nf * 0.29'
+ pd='2*int((nf+1)/2) * (W/nf + 0.29)' ps='2*int((nf+2)/2) * (W/nf + 0.29)' nrd='0.29 / W' nrs='0.29 / W'
+ sa=0 sb=0 sd=0 mult=1 m=1
XMd17 VP VP net3 VDD sky130_fd_pr__pfet_01v8 L=0.6 W=1.5 nf=1 ad='int((nf+1)/2) * W/nf * 0.29' as='int((nf+2)/2) * W/nf * 0.29'
+ pd='2*int((nf+1)/2) * (W/nf + 0.29)' ps='2*int((nf+2)/2) * (W/nf + 0.29)' nrd='0.29 / W' nrs='0.29 / W'
+ sa=0 sb=0 sd=0 mult=1 m=1
XM3a net5 net11 nVout GND sky130_fd_pr__nfet_01v8 L=0.6 W=1.5 nf=1 ad='int((nf+1)/2) * W/nf * 0.29' as='int((nf+2)/2) * W/nf * 0.29'
+ pd='2*int((nf+1)/2) * (W/nf + 0.29)' ps='2*int((nf+2)/2) * (W/nf + 0.29)' nrd='0.29 / W' nrs='0.29 / W'
+ sa=0 sb=0 sd=0 mult=1 m=1
XM4a net11 net11 net4 GND sky130_fd_pr__nfet_01v8 L=0.6 W=1.5 nf=1 ad='int((nf+1)/2) * W/nf * 0.29' as='int((nf+2)/2) * W/nf * 0.29'
+ pd='2*int((nf+1)/2) * (W/nf + 0.29)' ps='2*int((nf+2)/2) * (W/nf + 0.29)' nrd='0.29 / W' nrs='0.29 / W'
+ sa=0 sb=0 sd=0 mult=1 m=1
XM3b nVout net11 net5 GND sky130_fd_pr__nfet_01v8 L=0.6 W=1.5 nf=1 ad='int((nf+1)/2) * W/nf * 0.29' as='int((nf+2)/2) * W/nf * 0.29'
+ pd='2*int((nf+1)/2) * (W/nf + 0.29)' ps='2*int((nf+2)/2) * (W/nf + 0.29)' nrd='0.29 / W' nrs='0.29 / W'
+ sa=0 sb=0 sd=0 mult=1 m=1
XM4b net4 net11 net11 GND sky130_fd_pr__nfet_01v8 L=0.6 W=1.5 nf=1 ad='int((nf+1)/2) * W/nf * 0.29' as='int((nf+2)/2) * W/nf * 0.29'
+ pd='2*int((nf+1)/2) * (W/nf + 0.29)' ps='2*int((nf+2)/2) * (W/nf + 0.29)' nrd='0.29 / W' nrs='0.29 / W'
+ sa=0 sb=0 sd=0 mult=1 m=1
XMd19 VN VN net4 GND sky130_fd_pr__nfet_01v8 L=0.6 W=1.5 nf=1 ad='int((nf+1)/2) * W/nf * 0.29' as='int((nf+2)/2) * W/nf * 0.29'
+ pd='2*int((nf+1)/2) * (W/nf + 0.29)' ps='2*int((nf+2)/2) * (W/nf + 0.29)' nrd='0.29 / W' nrs='0.29 / W'
+ sa=0 sb=0 sd=0 mult=1 m=1
XMd20 net4 VN VN GND sky130_fd_pr__nfet_01v8 L=0.6 W=1.5 nf=1 ad='int((nf+1)/2) * W/nf * 0.29' as='int((nf+2)/2) * W/nf * 0.29'
+ pd='2*int((nf+1)/2) * (W/nf + 0.29)' ps='2*int((nf+2)/2) * (W/nf + 0.29)' nrd='0.29 / W' nrs='0.29 / W'
+ sa=0 sb=0 sd=0 mult=1 m=1
XM2 Vout nVout VN GND sky130_fd_pr__nfet_01v8 L=0.15 W=6 nf=1 ad='int((nf+1)/2) * W/nf * 0.29' as='int((nf+2)/2) * W/nf * 0.29'
+ pd='2*int((nf+1)/2) * (W/nf + 0.29)' ps='2*int((nf+2)/2) * (W/nf + 0.29)' nrd='0.29 / W' nrs='0.29 / W'
+ sa=0 sb=0 sd=0 mult=1 m=1
XM23 VP nVout Vout VDD sky130_fd_pr__pfet_01v8 L=0.15 W=12 nf=1 ad='int((nf+1)/2) * W/nf * 0.29' as='int((nf+2)/2) * W/nf * 0.29'
+ pd='2*int((nf+1)/2) * (W/nf + 0.29)' ps='2*int((nf+2)/2) * (W/nf + 0.29)' nrd='0.29 / W' nrs='0.29 / W'
+ sa=0 sb=0 sd=0 mult=1 m=1
.ends


* expanding   symbol:  /home/jonah/VLSI/final/amux.sym # of pins=6
** sym_path: analog/amux.sym
** sch_path: analog/amux.sch
.subckt amux A B Out VP VN C
*.iopin VN
*.iopin VP
*.ipin C
*.ipin A
*.ipin B
*.opin Out
XM1 B net1 Out VDD sky130_fd_pr__pfet_01v8 L=0.15 W=1 nf=1 ad='int((nf+1)/2) * W/nf * 0.29' as='int((nf+2)/2) * W/nf * 0.29'
+ pd='2*int((nf+1)/2) * (W/nf + 0.29)' ps='2*int((nf+2)/2) * (W/nf + 0.29)' nrd='0.29 / W' nrs='0.29 / W'
+ sa=0 sb=0 sd=0 mult=1 m=1
XM2 Out C B GND sky130_fd_pr__nfet_01v8 L=0.15 W=1 nf=1 ad='int((nf+1)/2) * W/nf * 0.29' as='int((nf+2)/2) * W/nf * 0.29'
+ pd='2*int((nf+1)/2) * (W/nf + 0.29)' ps='2*int((nf+2)/2) * (W/nf + 0.29)' nrd='0.29 / W' nrs='0.29 / W'
+ sa=0 sb=0 sd=0 mult=1 m=1
XM3 Out C A VDD sky130_fd_pr__pfet_01v8 L=0.15 W=1 nf=1 ad='int((nf+1)/2) * W/nf * 0.29' as='int((nf+2)/2) * W/nf * 0.29'
+ pd='2*int((nf+1)/2) * (W/nf + 0.29)' ps='2*int((nf+2)/2) * (W/nf + 0.29)' nrd='0.29 / W' nrs='0.29 / W'
+ sa=0 sb=0 sd=0 mult=1 m=1
XM4 A net1 Out GND sky130_fd_pr__nfet_01v8 L=0.15 W=1 nf=1 ad='int((nf+1)/2) * W/nf * 0.29' as='int((nf+2)/2) * W/nf * 0.29'
+ pd='2*int((nf+1)/2) * (W/nf + 0.29)' ps='2*int((nf+2)/2) * (W/nf + 0.29)' nrd='0.29 / W' nrs='0.29 / W'
+ sa=0 sb=0 sd=0 mult=1 m=1
XM5 net1 C VP VDD sky130_fd_pr__pfet_01v8 L=0.15 W=1 nf=1 ad='int((nf+1)/2) * W/nf * 0.29' as='int((nf+2)/2) * W/nf * 0.29'
+ pd='2*int((nf+1)/2) * (W/nf + 0.29)' ps='2*int((nf+2)/2) * (W/nf + 0.29)' nrd='0.29 / W' nrs='0.29 / W'
+ sa=0 sb=0 sd=0 mult=1 m=1
XM6 VN C net1 GND sky130_fd_pr__nfet_01v8 L=0.15 W=1 nf=1 ad='int((nf+1)/2) * W/nf * 0.29' as='int((nf+2)/2) * W/nf * 0.29'
+ pd='2*int((nf+1)/2) * (W/nf + 0.29)' ps='2*int((nf+2)/2) * (W/nf + 0.29)' nrd='0.29 / W' nrs='0.29 / W'
+ sa=0 sb=0 sd=0 mult=1 m=1
.ends

.GLOBAL VDD
.GLOBAL GND
.end
